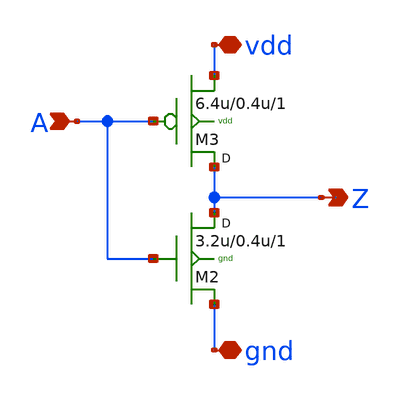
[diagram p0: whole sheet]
** sch_path: sram_4_16_scn4m/pinv_11.sch
**.subckt pinv_11 A Z vdd gnd
*.ipin A
*.opin Z
*.iopin vdd
*.iopin gnd
M2 Z A gnd gnd n w=3.2u l=0.4u m=1
M3 Z A vdd vdd p w=6.4u l=0.4u m=1
**.ends
.end
